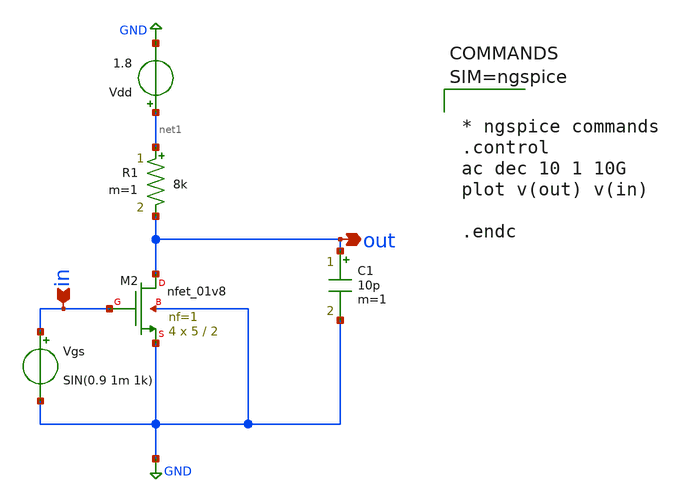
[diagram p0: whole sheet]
** sch_path: xschem/mos_ac.sch
**.subckt mos_ac in out
*.ipin in
*.opin out
XM2 out in GND GND sky130_fd_pr__nfet_01v8 L=2 W=5 nf=1 ad='int((1 + 1)/2) * 5 / 1 * 0.29' as='int((1 + 2)/2) * 5 / 1 * 0.29'
+ pd='2*int((1 + 1)/2) * (5 / 1 + 0.29)' ps='2*int((1 + 2)/2) * (5 / 1 + 0.29)' nrd='0.29 / 5 ' nrs='0.29 / 5 '
+ sa=0 sb=0 sd=0 mult=4 m=4
Vgs in GND SIN(0.9 1m 1k)
C1 out GND 10p m=1
R1 net1 out 8k m=1
Vdd net1 GND 1.8
**** begin user architecture code

** opencircuitdesign pdks install
.lib $::SKYWATER_MODELS/sky130.lib.spice tt




* ngspice commands
.control
ac dec 10 1 10G
plot v(out) v(in)

.endc



**** end user architecture code
**.ends
.GLOBAL GND
.end
